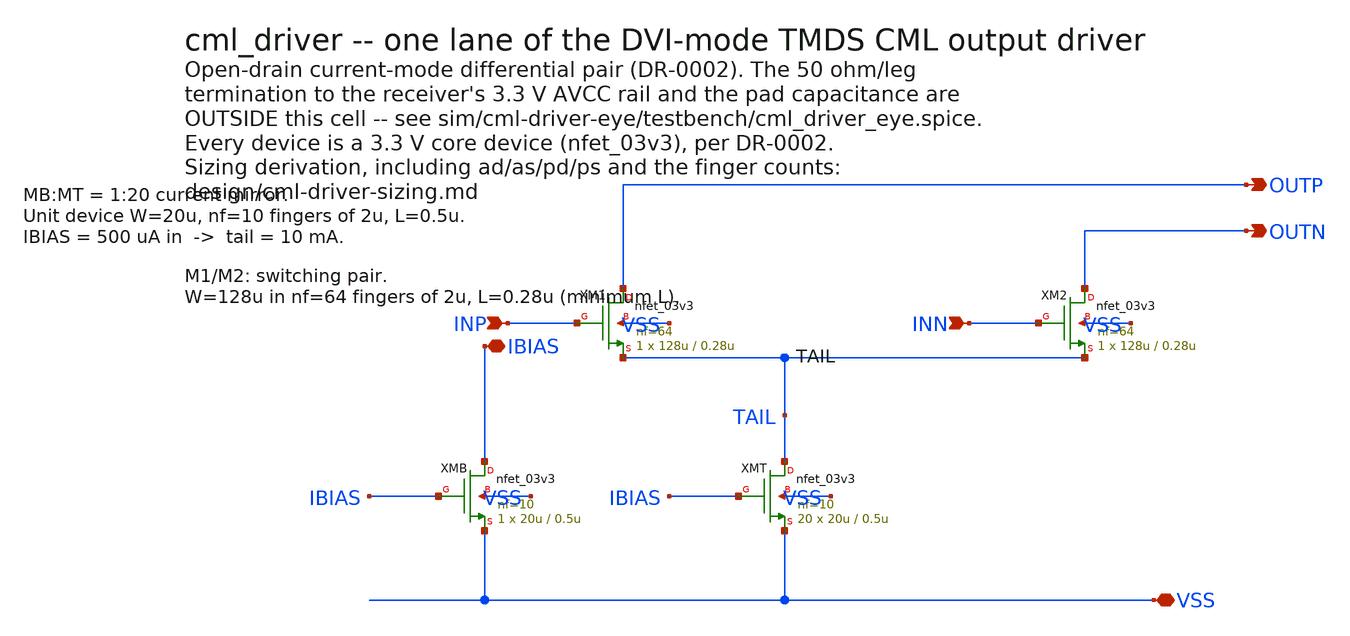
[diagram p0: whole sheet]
** sch_path: design/cml_driver.sch
**.subckt cml_driver INP INN OUTP OUTN IBIAS VSS
*.ipin INP
*.ipin INN
*.opin OUTP
*.opin OUTN
*.iopin IBIAS
*.iopin VSS
XM1 OUTP INP TAIL VSS nfet_03v3 L=0.28u W=128u nf=64 ad=11.52p as=11.88p pd=139.52u ps=143.88u
+ nrd=1.40625m nrs=1.40625m sa=0 sb=0 sd=0 m=1
XM2 OUTN INN TAIL VSS nfet_03v3 L=0.28u W=128u nf=64 ad=11.52p as=11.88p pd=139.52u ps=143.88u
+ nrd=1.40625m nrs=1.40625m sa=0 sb=0 sd=0 m=1
XMT TAIL IBIAS VSS VSS nfet_03v3 L=0.5u W=20u nf=10 ad=1.8p as=2.16p pd=21.8u ps=26.16u nrd=9m
+ nrs=9m sa=0 sb=0 sd=0 m=20
XMB IBIAS IBIAS VSS VSS nfet_03v3 L=0.5u W=20u nf=10 ad=1.8p as=2.16p pd=21.8u ps=26.16u nrd=9m
+ nrs=9m sa=0 sb=0 sd=0 m=1
**.ends
.end
